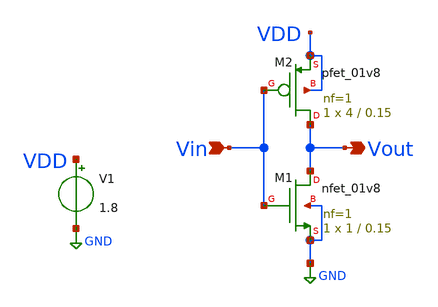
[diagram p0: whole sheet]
** sch_path: xschem/Inverter.sch
**.subckt Inverter Vin Vout
*.ipin Vin
*.opin Vout
XM1 Vout Vin GND GND sky130_fd_pr__nfet_01v8 L=0.15 W=1 nf=1 ad='int((nf+1)/2) * W/nf * 0.29' as='int((nf+2)/2) * W/nf * 0.29'
+ pd='2*int((nf+1)/2) * (W/nf + 0.29)' ps='2*int((nf+2)/2) * (W/nf + 0.29)' nrd='0.29 / W' nrs='0.29 / W'
+ sa=0 sb=0 sd=0 mult=1 m=1
XM2 Vout Vin VDD VDD sky130_fd_pr__pfet_01v8 L=0.15 W=4 nf=1 ad='int((nf+1)/2) * W/nf * 0.29' as='int((nf+2)/2) * W/nf * 0.29'
+ pd='2*int((nf+1)/2) * (W/nf + 0.29)' ps='2*int((nf+2)/2) * (W/nf + 0.29)' nrd='0.29 / W' nrs='0.29 / W'
+ sa=0 sb=0 sd=0 mult=1 m=1
V1 VDD GND 1.8
**.ends
.GLOBAL GND
.end
